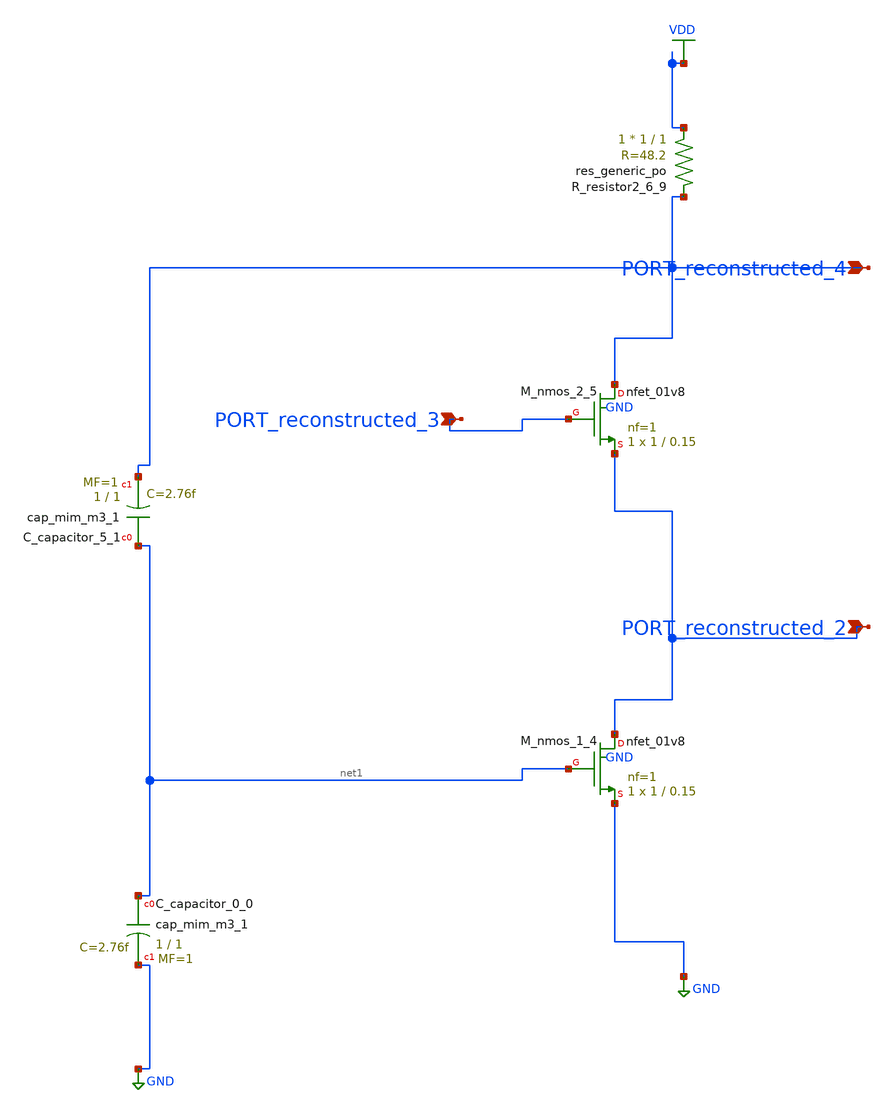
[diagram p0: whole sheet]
** sch_path: schematics/AMSNet/541.sch
**.subckt 541 PORT_reconstructed_3 PORT_reconstructed_4 PORT_reconstructed_2
*.ipin PORT_reconstructed_3
*.ipin PORT_reconstructed_4
*.ipin PORT_reconstructed_2
XC_capacitor_0_0 net1 GND sky130_fd_pr__cap_mim_m3_1 W=1 L=1 MF=1 m=1
XC_capacitor_5_1 net1 PORT_reconstructed_4 sky130_fd_pr__cap_mim_m3_1 W=1 L=1 MF=1 m=1
XM_nmos_1_4 PORT_reconstructed_2 net1 GND GND sky130_fd_pr__nfet_01v8 L=0.15 W=1 nf=1 ad='int((1 + 1)/2) * 1 / 1 * 0.29'
+ as='int((1 + 2)/2) * 1 / 1 * 0.29' pd='2*int((1 + 1)/2) * (1 / 1 + 0.29)' ps='2*int((1 + 2)/2) * (1 / 1 + 0.29)'
+ nrd='0.29 / 1 ' nrs='0.29 / 1 ' sa=0 sb=0 sd=0 mult=1 m=1
XM_nmos_2_5 PORT_reconstructed_4 PORT_reconstructed_3 PORT_reconstructed_2 GND sky130_fd_pr__nfet_01v8
+ L=0.15 W=1 nf=1 ad='int((1 + 1)/2) * 1 / 1 * 0.29' as='int((1 + 2)/2) * 1 / 1 * 0.29' pd='2*int((1 + 1)/2) * (1 / 1 + 0.29)'
+ ps='2*int((1 + 2)/2) * (1 / 1 + 0.29)' nrd='0.29 / 1 ' nrs='0.29 / 1 ' sa=0 sb=0 sd=0 mult=1 m=1
XR_resistor2_6_9 VDD PORT_reconstructed_4 sky130_fd_pr__res_generic_po W=1 L=1 m=1
**.ends
.GLOBAL GND
.GLOBAL VDD
.end
